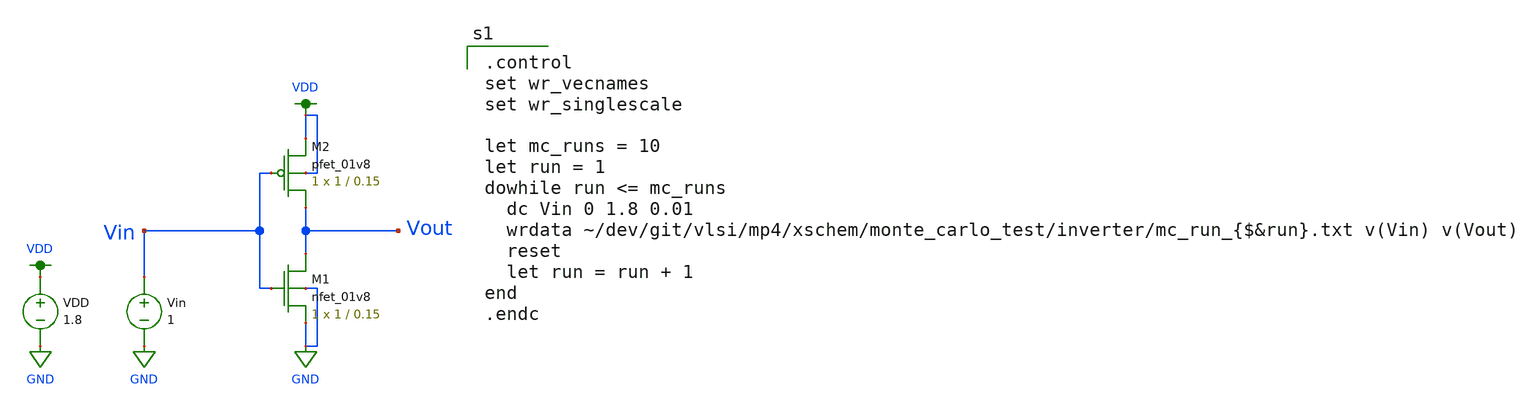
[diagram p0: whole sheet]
** sch_path: mp4/xschem/monte_carlo_test/inverter.sch
**.subckt inverter
Vin Vin GND 1
VDD VDD GND 1.8
XM2 Vout Vin VDD VDD sky130_fd_pr__pfet_01v8 L=0.15 W=1 nf=1 ad='int((nf+1)/2) * W/nf * 0.29' as='int((nf+2)/2) * W/nf * 0.29'
+ pd='2*int((nf+1)/2) * (W/nf + 0.29)' ps='2*int((nf+2)/2) * (W/nf + 0.29)' nrd='0.29 / W' nrs='0.29 / W'
+ sa=0 sb=0 sd=0 mult=1 m=1
XM1 Vout Vin GND GND sky130_fd_pr__nfet_01v8 L=0.15 W=1 nf=1 ad='int((nf+1)/2) * W/nf * 0.29' as='int((nf+2)/2) * W/nf * 0.29'
+ pd='2*int((nf+1)/2) * (W/nf + 0.29)' ps='2*int((nf+2)/2) * (W/nf + 0.29)' nrd='0.29 / W' nrs='0.29 / W'
+ sa=0 sb=0 sd=0 mult=1 m=1
**** begin user architecture code

.option wnflag=1
.param MC_SWITCH=1.0
.lib ~/skywater/skywater-pdk/libraries/sky130_fd_pr_ngspice/latest/models/sky130.lib.spice tt


.control
set wr_vecnames
set wr_singlescale

let mc_runs = 10
let run = 1
dowhile run <= mc_runs
  dc Vin 0 1.8 0.01
  wrdata ~/dev/git/vlsi/mp4/xschem/monte_carlo_test/inverter/mc_run_{$&run}.txt v(Vin) v(Vout)
  reset
  let run = run + 1
end
.endc

**** end user architecture code
**.ends
.GLOBAL GND
.GLOBAL VDD
.end
